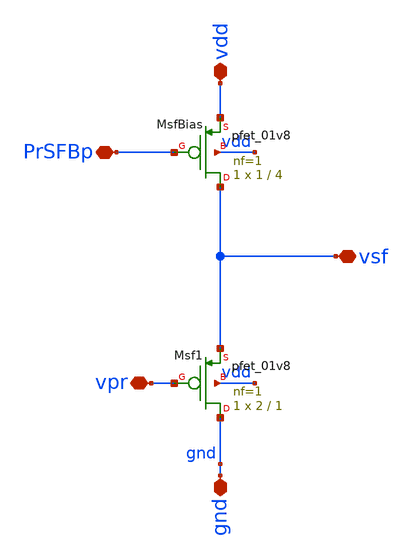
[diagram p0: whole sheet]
** sch_path: analog/xschem/PixelSourceFollower.sch
**.subckt PixelSourceFollower gnd PrSFBp vpr vsf vdd
*.iopin gnd
*.iopin PrSFBp
*.iopin vpr
*.iopin vsf
*.iopin vdd
XMsfBias vsf PrSFBp vdd vdd sky130_fd_pr__pfet_01v8 L=4 W=1 nf=1 ad='int((1 + 1)/2) * 1 / 1 * 0.29' as='int((1 + 2)/2) * 1 / 1 * 0.29'
+ pd='2*int((1 + 1)/2) * (1 / 1 + 0.29)' ps='2*int((1 + 2)/2) * (1 / 1 + 0.29)' nrd='0.29 / 1 ' nrs='0.29 / 1 '
+ sa=0 sb=0 sd=0 mult=1 m=1
XMsf1 gnd vpr vsf vdd sky130_fd_pr__pfet_01v8 L=1 W=2 nf=1 ad='int((1 + 1)/2) * 2 / 1 * 0.29' as='int((1 + 2)/2) * 2 / 1 * 0.29'
+ pd='2*int((1 + 1)/2) * (2 / 1 + 0.29)' ps='2*int((1 + 2)/2) * (2 / 1 + 0.29)' nrd='0.29 / 2 ' nrs='0.29 / 2 '
+ sa=0 sb=0 sd=0 mult=1 m=1
**.ends
.end
